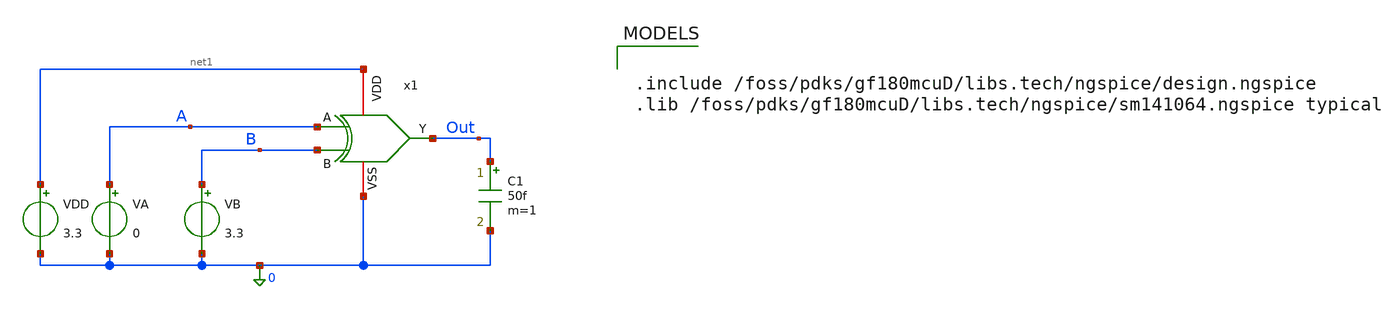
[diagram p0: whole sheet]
** sch_path: src/UN_PFD_GF180mcuD/work/UN_stdXOR_0_gf180mcuD_TB.sch
**.subckt UN_stdXOR_0_gf180mcuD_TB
VA A 0 0
VB B 0 3.3
C1 Out 0 50f m=1
VDD net1 0 3.3
x1 net1 A Out B 0 UN_stdXOR_0_gf180mcuD
**** begin user architecture code



.control
save all *TODO: find out what this does.
set filetype=ascii

** Define Input Signal Properties.
** let allows calculations. set does not.

let fsig = 0.1e8
let tper = 1/fsig
let tfr = 0.01*tper
let ton = 0.5*tper-2*tfr
let tdel= 0.2*tper

** Define the parameters for Transient Analysis
** For transient Analysis, you have 2 parameters typically, How long to run sim and step size.

let tstop = 5*tper
let tstep = 0.001*tper

** Set the input sources with these parameters.
** VDD is already stable, but you can choose to simulate it separately.
** You use alter command to edit the default properties of the sources

alter @VA[DC] = 0.0
alter @VB[DC] = 3.3
alter @VA[PULSE] = [ 0 3.3 0 $&tfr $&tfr $&ton $&tper ]
alter @VB[PULSE] = [ 0 3.3 $&tdel $&tfr $&tfr $&ton $&tper ]

**** list of simulations to perform
**** The $& evaluates expressions and converts results to string because parameters are expected to
*+ be string

op
tran $&tstep $&tstop

** plots
setplot tran1
let vout = v(out)
let va= v(a)
let vb= v(b)

let ivdd = vdd#branch *1e3 * -1

plot vout va vb

setplot op1

write /foss/designs/un_basicpll_gf180mcud/un_pfd_gf180mcud/sim/stdxor_tb.raw tran1.all

.endc



.include /foss/pdks/gf180mcuD/libs.tech/ngspice/design.ngspice
.lib /foss/pdks/gf180mcuD/libs.tech/ngspice/sm141064.ngspice typical

**** end user architecture code
**.ends

* expanding   symbol:
*+  /foss/designs/UN_BasicPLL_GF180mcuD/UN_PFD_GF180mcuD/work/UN_stdXOR_0_gf180mcuD.sym # of pins=5
** sym_path: src/UN_PFD_GF180mcuD/work/UN_stdXOR_0_gf180mcuD.sym
** sch_path: src/UN_PFD_GF180mcuD/work/UN_stdXOR_0_gf180mcuD.sch
.subckt UN_stdXOR_0_gf180mcuD VDD A Y B VSS
*.iopin VDD
*.iopin VSS
*.ipin A
*.ipin B
*.opin Y
XM1 net1 A VSS VSS nfet_03v3 L=0.28u W=0.22u nf=1 ad='int((nf+1)/2) * W/nf * 0.18u' as='int((nf+2)/2) * W/nf * 0.18u'
+ pd='2*int((nf+1)/2) * (W/nf + 0.18u)' ps='2*int((nf+2)/2) * (W/nf + 0.18u)' nrd='0.18u / W' nrs='0.18u / W'
+ sa=0 sb=0 sd=0 m=1
XM2 net1 B VSS VSS nfet_03v3 L=0.28u W=0.22u nf=1 ad='int((nf+1)/2) * W/nf * 0.18u' as='int((nf+2)/2) * W/nf * 0.18u'
+ pd='2*int((nf+1)/2) * (W/nf + 0.18u)' ps='2*int((nf+2)/2) * (W/nf + 0.18u)' nrd='0.18u / W' nrs='0.18u / W'
+ sa=0 sb=0 sd=0 m=1
XM3 Y net1 VSS VSS nfet_03v3 L=0.28u W=0.22u nf=1 ad='int((nf+1)/2) * W/nf * 0.18u' as='int((nf+2)/2) * W/nf * 0.18u'
+ pd='2*int((nf+1)/2) * (W/nf + 0.18u)' ps='2*int((nf+2)/2) * (W/nf + 0.18u)' nrd='0.18u / W' nrs='0.18u / W'
+ sa=0 sb=0 sd=0 m=1
XM4 Y A net4 VSS nfet_03v3 L=0.28u W=0.22u nf=1 ad='int((nf+1)/2) * W/nf * 0.18u' as='int((nf+2)/2) * W/nf * 0.18u'
+ pd='2*int((nf+1)/2) * (W/nf + 0.18u)' ps='2*int((nf+2)/2) * (W/nf + 0.18u)' nrd='0.18u / W' nrs='0.18u / W'
+ sa=0 sb=0 sd=0 m=1
XM5 net4 B VSS VSS nfet_03v3 L=0.28u W=0.22u nf=1 ad='int((nf+1)/2) * W/nf * 0.18u' as='int((nf+2)/2) * W/nf * 0.18u'
+ pd='2*int((nf+1)/2) * (W/nf + 0.18u)' ps='2*int((nf+2)/2) * (W/nf + 0.18u)' nrd='0.18u / W' nrs='0.18u / W'
+ sa=0 sb=0 sd=0 m=1
XM6 net1 B net2 VDD pfet_03v3 L=0.28u W=0.22u nf=1 ad='int((nf+1)/2) * W/nf * 0.18u' as='int((nf+2)/2) * W/nf * 0.18u'
+ pd='2*int((nf+1)/2) * (W/nf + 0.18u)' ps='2*int((nf+2)/2) * (W/nf + 0.18u)' nrd='0.18u / W' nrs='0.18u / W'
+ sa=0 sb=0 sd=0 m=1
XM7 net2 A VDD VDD pfet_03v3 L=0.28u W=0.22u nf=1 ad='int((nf+1)/2) * W/nf * 0.18u' as='int((nf+2)/2) * W/nf * 0.18u'
+ pd='2*int((nf+1)/2) * (W/nf + 0.18u)' ps='2*int((nf+2)/2) * (W/nf + 0.18u)' nrd='0.18u / W' nrs='0.18u / W'
+ sa=0 sb=0 sd=0 m=1
XM8 net3 net1 VDD VDD pfet_03v3 L=0.28u W=0.22u nf=1 ad='int((nf+1)/2) * W/nf * 0.18u' as='int((nf+2)/2) * W/nf * 0.18u'
+ pd='2*int((nf+1)/2) * (W/nf + 0.18u)' ps='2*int((nf+2)/2) * (W/nf + 0.18u)' nrd='0.18u / W' nrs='0.18u / W'
+ sa=0 sb=0 sd=0 m=1
XM9 Y A net3 VDD pfet_03v3 L=0.28u W=0.22u nf=1 ad='int((nf+1)/2) * W/nf * 0.18u' as='int((nf+2)/2) * W/nf * 0.18u'
+ pd='2*int((nf+1)/2) * (W/nf + 0.18u)' ps='2*int((nf+2)/2) * (W/nf + 0.18u)' nrd='0.18u / W' nrs='0.18u / W'
+ sa=0 sb=0 sd=0 m=1
XM10 Y B net3 VDD pfet_03v3 L=0.28u W=0.22u nf=1 ad='int((nf+1)/2) * W/nf * 0.18u' as='int((nf+2)/2) * W/nf * 0.18u'
+ pd='2*int((nf+1)/2) * (W/nf + 0.18u)' ps='2*int((nf+2)/2) * (W/nf + 0.18u)' nrd='0.18u / W' nrs='0.18u / W'
+ sa=0 sb=0 sd=0 m=1
.ends

.end
